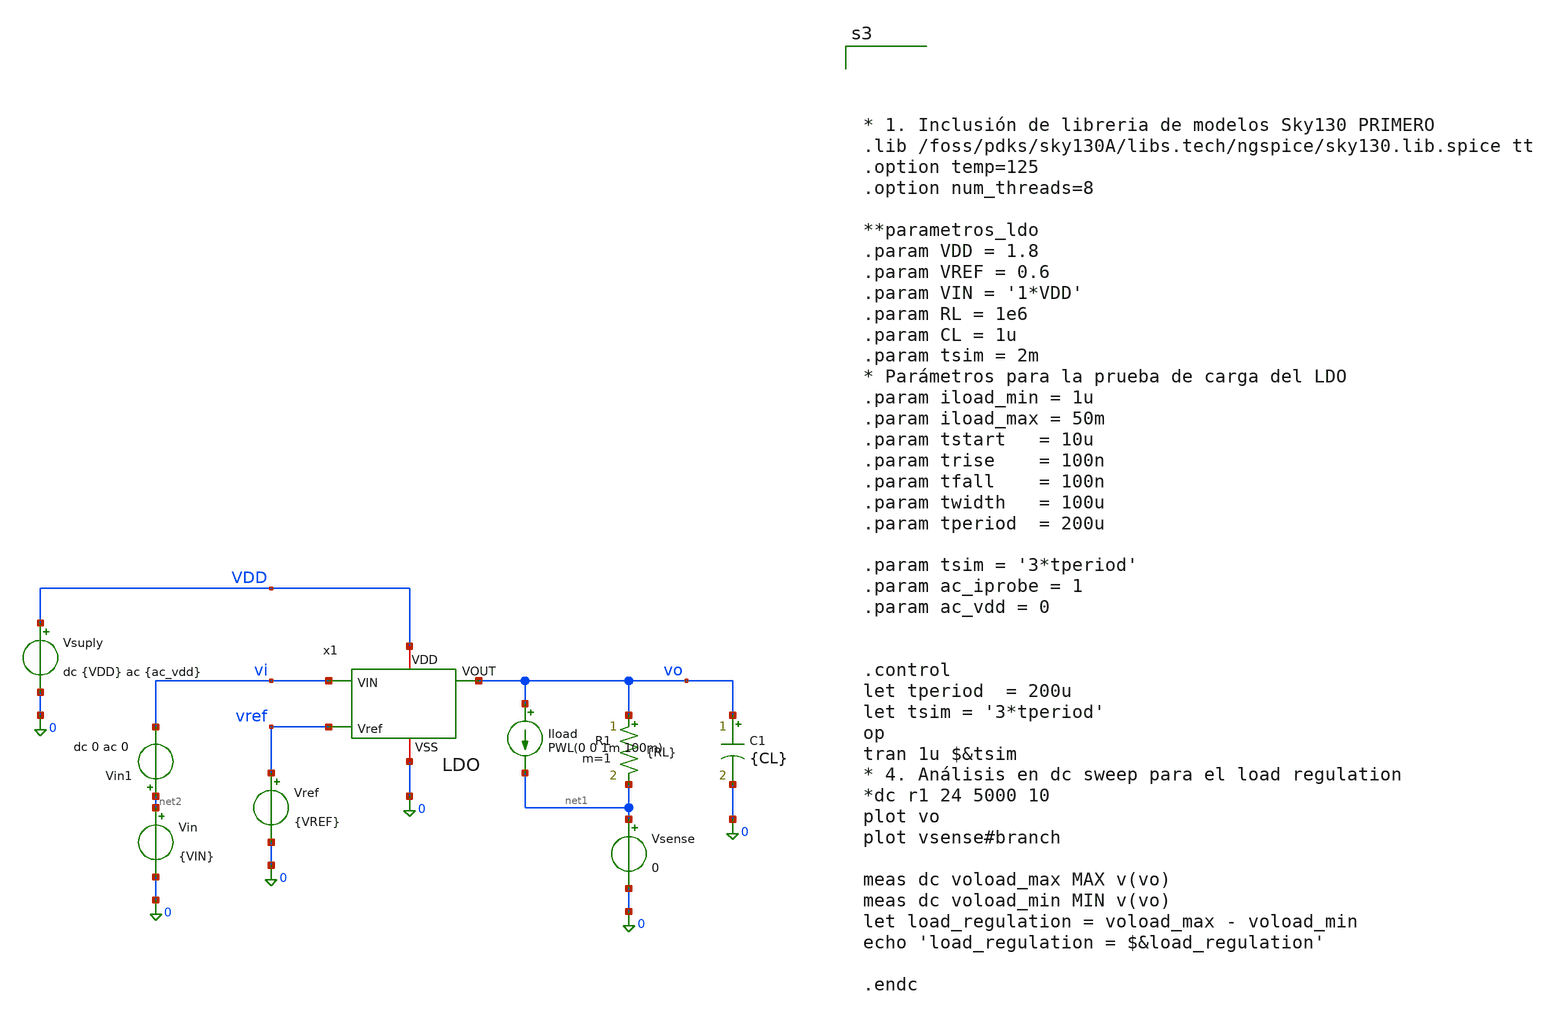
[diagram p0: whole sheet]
** sch_path: untitled.sch
**.subckt untitled
Vsuply VDD 0 dc {VDD} ac {ac_vdd}
Vref vref 0 {VREF}
Vin net2 0 {VIN}
R1 vo net1 {RL} m=1
C1 vo 0 {CL} m=1
Vsense net1 0 0
Vin1 net2 vi dc 0 ac 0
x1 vi vo VDD vref 0 LDO
Iload vo net1 PWL(0 0 1m 100m)
**** begin user architecture code




* 1. Inclusión de libreria de modelos Sky130 PRIMERO
.lib /foss/pdks/sky130A/libs.tech/ngspice/sky130.lib.spice tt
.option temp=125
.option num_threads=8

**parametros_ldo
.param VDD = 1.8
.param VREF = 0.6
.param VIN = '1*VDD'
.param RL = 1e6
.param CL = 1u
.param tsim = 2m
* Parámetros para la prueba de carga del LDO
.param iload_min = 1u
.param iload_max = 50m
.param tstart   = 10u
.param trise    = 100n
.param tfall    = 100n
.param twidth   = 100u
.param tperiod  = 200u

.param tsim = '3*tperiod'
.param ac_iprobe = 1
.param ac_vdd = 0


.control
let tperiod  = 200u
let tsim = '3*tperiod'
op
tran 1u $&tsim
* 4. Análisis en dc sweep para el load regulation
*dc r1 24 5000 10
plot vo
plot vsense#branch

meas dc voload_max MAX v(vo)
meas dc voload_min MIN v(vo)
let load_regulation = voload_max - voload_min
echo 'load_regulation = $&load_regulation'

.endc



**** end user architecture code
**.ends

* expanding   symbol:  /foss/designs/LDO-sky130/xschem/LDO.sym # of pins=5
** sym_path: xschem/LDO.sym
** sch_path: xschem/LDO.sch
.subckt LDO VIN VOUT VDD Vref VSS
*.ipin VIN
*.iopin VDD
*.opin VOUT
*.ipin Vref
*.iopin VSS
V1 vre2 Vre 0 ac {ac_iprobe}
x1 VDD Vgp Vref vre2 VSS Vgn_bias OTA
XC1 VOUT Vre sky130_fd_pr__cap_mim_m3_2 W=27 L=25 MF=1 m=1
XM1 VOUT Vgp VIN VDD sky130_fd_pr__pfet_01v8_lvt L=0.5 W=250 nf=100 ad='int((100 + 1)/2) * 250 / 100 * 0.29'
+ as='int((100 + 2)/2) * 250 / 100 * 0.29' pd='2*int((100 + 1)/2) * (250 / 100 + 0.29)' ps='2*int((100 + 2)/2) * (250 / 100 + 0.29)'
+ nrd='0.29 / 250 ' nrs='0.29 / 250 ' sa=0 sb=0 sd=0 mult=5 m=5
x2 VDD Vgn_bias VSS self_bias
R8 VOUT Vre {109k*(1+rsh_var)} m=1
R9 Vre VSS {109k*(1+rsh_var)} m=1
.ends


* expanding   symbol:  /foss/designs/LDO-sky130/xschem/OTA.sym # of pins=6
** sym_path: xschem/OTA/OTA.sym
** sch_path: xschem/OTA/OTA.sch
.subckt OTA VDD VO_ota VIN_ota VIP_ota VSS VGN
*.ipin VIN_ota
*.opin VO_ota
*.iopin VSS
*.iopin VDD
*.ipin VIP_ota
*.iopin VGN
XMpr vo1 vd VSS VSS sky130_fd_pr__nfet_01v8 L=1 W=6 nf=4 ad='int((4 + 1)/2) * 6 / 4 * 0.29' as='int((4 + 2)/2) * 6 / 4 * 0.29'
+ pd='2*int((4 + 1)/2) * (6 / 4 + 0.29)' ps='2*int((4 + 2)/2) * (6 / 4 + 0.29)' nrd='0.29 / 6 ' nrs='0.29 / 6 '
+ sa=0 sb=0 sd=0 mult=1 m=1
XMnr vd vd VSS VSS sky130_fd_pr__nfet_01v8 L=1 W=6 nf=4 ad='int((4 + 1)/2) * 6 / 4 * 0.29' as='int((4 + 2)/2) * 6 / 4 * 0.29'
+ pd='2*int((4 + 1)/2) * (6 / 4 + 0.29)' ps='2*int((4 + 2)/2) * (6 / 4 + 0.29)' nrd='0.29 / 6 ' nrs='0.29 / 6 '
+ sa=0 sb=0 sd=0 mult=1 m=1
XMo VO_ota vo1 VSS VSS sky130_fd_pr__nfet_01v8 L=2 W=8 nf=8 ad='int((8 + 1)/2) * 8 / 8 * 0.29' as='int((8 + 2)/2) * 8 / 8 * 0.29'
+ pd='2*int((8 + 1)/2) * (8 / 8 + 0.29)' ps='2*int((8 + 2)/2) * (8 / 8 + 0.29)' nrd='0.29 / 8 ' nrs='0.29 / 8 '
+ sa=0 sb=0 sd=0 mult=1 m=1
XMrc2 VO_ota vgp VDD VDD sky130_fd_pr__pfet_01v8_lvt L=2 W=50 nf=8 ad='int((8 + 1)/2) * 50 / 8 * 0.29'
+ as='int((8 + 2)/2) * 50 / 8 * 0.29' pd='2*int((8 + 1)/2) * (50 / 8 + 0.29)' ps='2*int((8 + 2)/2) * (50 / 8 + 0.29)'
+ nrd='0.29 / 50 ' nrs='0.29 / 50 ' sa=0 sb=0 sd=0 mult=1 m=1
XC1 VO_ota vmiler sky130_fd_pr__cap_mim_m3_2 W=44.6 L=56 MF=1 m=1
XMp vo1 VIP_ota vtail VDD sky130_fd_pr__pfet_01v8_lvt L=1 W=26 nf=4 ad='int((4 + 1)/2) * 26 / 4 * 0.29'
+ as='int((4 + 2)/2) * 26 / 4 * 0.29' pd='2*int((4 + 1)/2) * (26 / 4 + 0.29)' ps='2*int((4 + 2)/2) * (26 / 4 + 0.29)'
+ nrd='0.29 / 26 ' nrs='0.29 / 26 ' sa=0 sb=0 sd=0 mult=1 m=1
XMn vd VIN_ota vtail VDD sky130_fd_pr__pfet_01v8_lvt L=1 W=26 nf=4 ad='int((4 + 1)/2) * 26 / 4 * 0.29'
+ as='int((4 + 2)/2) * 26 / 4 * 0.29' pd='2*int((4 + 1)/2) * (26 / 4 + 0.29)' ps='2*int((4 + 2)/2) * (26 / 4 + 0.29)'
+ nrd='0.29 / 26 ' nrs='0.29 / 26 ' sa=0 sb=0 sd=0 mult=1 m=1
XMrc1 vtail vgp VDD VDD sky130_fd_pr__pfet_01v8_lvt L=1 W=50 nf=8 ad='int((8 + 1)/2) * 50 / 8 * 0.29'
+ as='int((8 + 2)/2) * 50 / 8 * 0.29' pd='2*int((8 + 1)/2) * (50 / 8 + 0.29)' ps='2*int((8 + 2)/2) * (50 / 8 + 0.29)'
+ nrd='0.29 / 50 ' nrs='0.29 / 50 ' sa=0 sb=0 sd=0 mult=1 m=1
XMr vgp vgp VDD VDD sky130_fd_pr__pfet_01v8_lvt L=1 W=12.5 nf=2 ad='int((2 + 1)/2) * 12.5 / 2 * 0.29'
+ as='int((2 + 2)/2) * 12.5 / 2 * 0.29' pd='2*int((2 + 1)/2) * (12.5 / 2 + 0.29)' ps='2*int((2 + 2)/2) * (12.5 / 2 + 0.29)'
+ nrd='0.29 / 12.5 ' nrs='0.29 / 12.5 ' sa=0 sb=0 sd=0 mult=1 m=1
XMnref vgp VGN VSS VSS sky130_fd_pr__nfet_01v8 L=1 W=8 nf=1 ad='int((1 + 1)/2) * 8 / 1 * 0.29' as='int((1 + 2)/2) * 8 / 1 * 0.29'
+ pd='2*int((1 + 1)/2) * (8 / 1 + 0.29)' ps='2*int((1 + 2)/2) * (8 / 1 + 0.29)' nrd='0.29 / 8 ' nrs='0.29 / 8 '
+ sa=0 sb=0 sd=0 mult=1 m=1
XR10 vo1 vmiler VSS sky130_fd_pr__res_xhigh_po_0p35 L=90.72 mult=1 m=1
.ends


* expanding   symbol:  /foss/designs/OSCAR/xschem/Iref/self_bias.sym # of pins=3
** sym_path: xschem/Iref/self_bias.sym
** sch_path: xschem/Iref/self_bias.sch
.subckt self_bias VDD VR VSS
*.iopin VR
*.iopin VDD
*.iopin VSS
XMp4 vgp_self vgp_self VDD VDD sky130_fd_pr__pfet_01v8_lvt L=1 W=30 nf=6 ad='int((6 + 1)/2) * 30 / 6 * 0.29'
+ as='int((6 + 2)/2) * 30 / 6 * 0.29' pd='2*int((6 + 1)/2) * (30 / 6 + 0.29)' ps='2*int((6 + 2)/2) * (30 / 6 + 0.29)'
+ nrd='0.29 / 30 ' nrs='0.29 / 30 ' sa=0 sb=0 sd=0 mult=1 m=1
XMp3 VDI vgp_self VDD VDD sky130_fd_pr__pfet_01v8_lvt L=1 W=30 nf=6 ad='int((6 + 1)/2) * 30 / 6 * 0.29'
+ as='int((6 + 2)/2) * 30 / 6 * 0.29' pd='2*int((6 + 1)/2) * (30 / 6 + 0.29)' ps='2*int((6 + 2)/2) * (30 / 6 + 0.29)'
+ nrd='0.29 / 30 ' nrs='0.29 / 30 ' sa=0 sb=0 sd=0 mult=1 m=1
XMs2 VDinv VR vp1 VDD sky130_fd_pr__pfet_01v8_lvt L=5 W=0.5 nf=1 ad='int((1 + 1)/2) * 0.5 / 1 * 0.29'
+ as='int((1 + 2)/2) * 0.5 / 1 * 0.29' pd='2*int((1 + 1)/2) * (0.5 / 1 + 0.29)' ps='2*int((1 + 2)/2) * (0.5 / 1 + 0.29)'
+ nrd='0.29 / 0.5 ' nrs='0.29 / 0.5 ' sa=0 sb=0 sd=0 mult=1 m=1
XMn2 vgp_self VDI VR VSS sky130_fd_pr__nfet_01v8 L=1 W=24 nf=6 ad='int((6 + 1)/2) * 24 / 6 * 0.29' as='int((6 + 2)/2) * 24 / 6 * 0.29'
+ pd='2*int((6 + 1)/2) * (24 / 6 + 0.29)' ps='2*int((6 + 2)/2) * (24 / 6 + 0.29)' nrd='0.29 / 24 ' nrs='0.29 / 24 '
+ sa=0 sb=0 sd=0 mult=1 m=1
XMn1 VDI VR VSS VSS sky130_fd_pr__nfet_01v8 L=1 W=5 nf=5 ad='int((5 + 1)/2) * 5 / 5 * 0.29' as='int((5 + 2)/2) * 5 / 5 * 0.29'
+ pd='2*int((5 + 1)/2) * (5 / 5 + 0.29)' ps='2*int((5 + 2)/2) * (5 / 5 + 0.29)' nrd='0.29 / 5 ' nrs='0.29 / 5 '
+ sa=0 sb=0 sd=0 mult=1 m=1
XMs3 VDinv VR VSS VSS sky130_fd_pr__nfet_01v8 L=1 W=20 nf=5 ad='int((5 + 1)/2) * 20 / 5 * 0.29' as='int((5 + 2)/2) * 20 / 5 * 0.29'
+ pd='2*int((5 + 1)/2) * (20 / 5 + 0.29)' ps='2*int((5 + 2)/2) * (20 / 5 + 0.29)' nrd='0.29 / 20 ' nrs='0.29 / 20 '
+ sa=0 sb=0 sd=0 mult=1 m=1
XMs1 vgp_self VDinv VSS VSS sky130_fd_pr__nfet_01v8 L=1 W=2 nf=2 ad='int((2 + 1)/2) * 2 / 2 * 0.29' as='int((2 + 2)/2) * 2 / 2 * 0.29'
+ pd='2*int((2 + 1)/2) * (2 / 2 + 0.29)' ps='2*int((2 + 2)/2) * (2 / 2 + 0.29)' nrd='0.29 / 2 ' nrs='0.29 / 2 '
+ sa=0 sb=0 sd=0 mult=1 m=1
XR11 VSS VR VSS sky130_fd_pr__res_xhigh_po_0p69 L=20.7 mult=1 m=1
XMs4 vp1 VR vp2 VDD sky130_fd_pr__pfet_01v8_lvt L=5 W=0.5 nf=1 ad='int((1 + 1)/2) * 0.5 / 1 * 0.29' as='int((1 + 2)/2) * 0.5 / 1 * 0.29'
+ pd='2*int((1 + 1)/2) * (0.5 / 1 + 0.29)' ps='2*int((1 + 2)/2) * (0.5 / 1 + 0.29)' nrd='0.29 / 0.5 ' nrs='0.29 / 0.5 '
+ sa=0 sb=0 sd=0 mult=1 m=1
XMs5 vp2 VR vp3 VDD sky130_fd_pr__pfet_01v8_lvt L=5 W=0.5 nf=1 ad='int((1 + 1)/2) * 0.5 / 1 * 0.29' as='int((1 + 2)/2) * 0.5 / 1 * 0.29'
+ pd='2*int((1 + 1)/2) * (0.5 / 1 + 0.29)' ps='2*int((1 + 2)/2) * (0.5 / 1 + 0.29)' nrd='0.29 / 0.5 ' nrs='0.29 / 0.5 '
+ sa=0 sb=0 sd=0 mult=1 m=1
XMs6 vp3 VR vp4 VDD sky130_fd_pr__pfet_01v8_lvt L=5 W=0.5 nf=1 ad='int((1 + 1)/2) * 0.5 / 1 * 0.29' as='int((1 + 2)/2) * 0.5 / 1 * 0.29'
+ pd='2*int((1 + 1)/2) * (0.5 / 1 + 0.29)' ps='2*int((1 + 2)/2) * (0.5 / 1 + 0.29)' nrd='0.29 / 0.5 ' nrs='0.29 / 0.5 '
+ sa=0 sb=0 sd=0 mult=1 m=1
XMs7 vp4 VR VDD VDD sky130_fd_pr__pfet_01v8_lvt L=5 W=0.5 nf=1 ad='int((1 + 1)/2) * 0.5 / 1 * 0.29' as='int((1 + 2)/2) * 0.5 / 1 * 0.29'
+ pd='2*int((1 + 1)/2) * (0.5 / 1 + 0.29)' ps='2*int((1 + 2)/2) * (0.5 / 1 + 0.29)' nrd='0.29 / 0.5 ' nrs='0.29 / 0.5 '
+ sa=0 sb=0 sd=0 mult=1 m=1
.ends

.end
